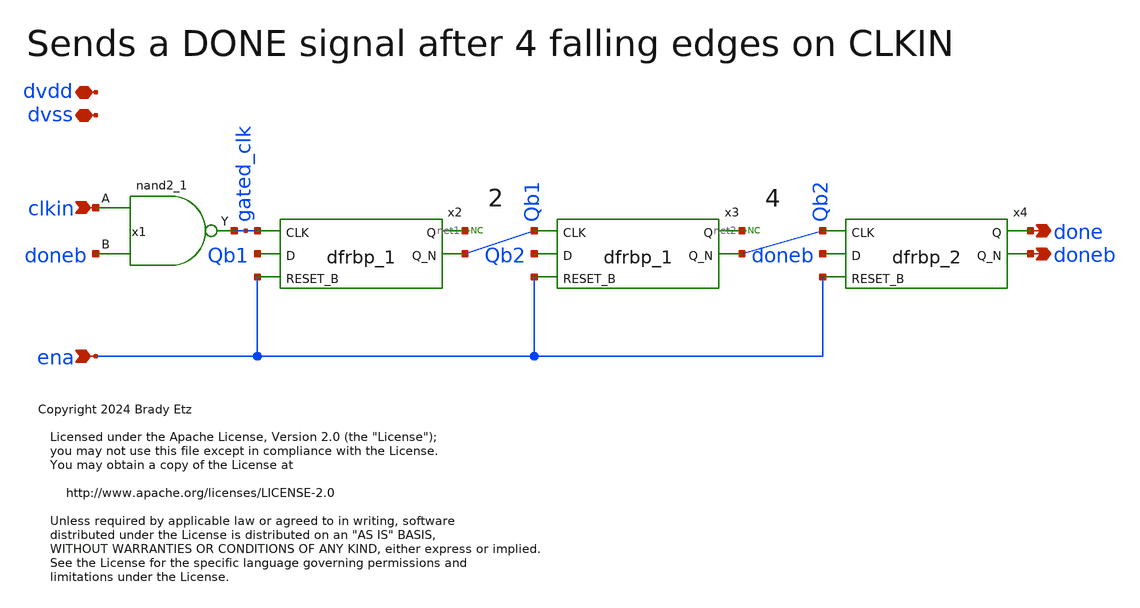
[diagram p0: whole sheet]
** sch_path: xschem/stby_rip_dly.sch
* Copyright 2024 Brady Etz
* Licensed under the Apache License, Version 2.0 (the "License");
**.subckt stby_rip_dly clkin ena done doneb dvdd dvss
*.ipin clkin
*.ipin ena
*.opin done
*.opin doneb
*.iopin dvdd
*.iopin dvss
x2 gated_clk Qb1 ena dvss dvss dvdd dvdd net1 Qb1 sky130_fd_sc_hd__dfrbp_1
x3 Qb1 Qb2 ena dvss dvss dvdd dvdd net2 Qb2 sky130_fd_sc_hd__dfrbp_1
x1 clkin doneb dvss dvss dvdd dvdd gated_clk sky130_fd_sc_hd__nand2_1
* noconn #net1
* noconn #net2
x4 Qb2 doneb ena dvss dvss dvdd dvdd done doneb sky130_fd_sc_hd__dfrbp_2
**.ends
.end
